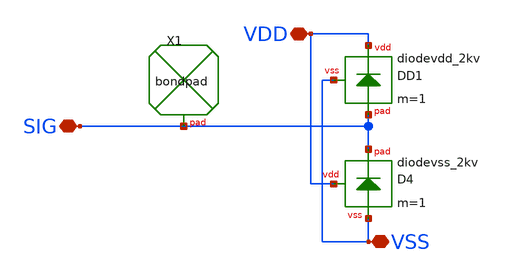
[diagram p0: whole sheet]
** sch_path: GPS_LNA/design_data/lvs/parts/pad_diode.sch
**.subckt pad_diode VDD VSS SIG
*.iopin VDD
*.iopin VSS
*.iopin SIG
XX1 SIG bondpad size=100u shape=0 padtype=0
XD1 VDD SIG VSS diodevdd_2kv m=1
XD4 VDD SIG VSS diodevss_2kv m=1
**.ends
.end
